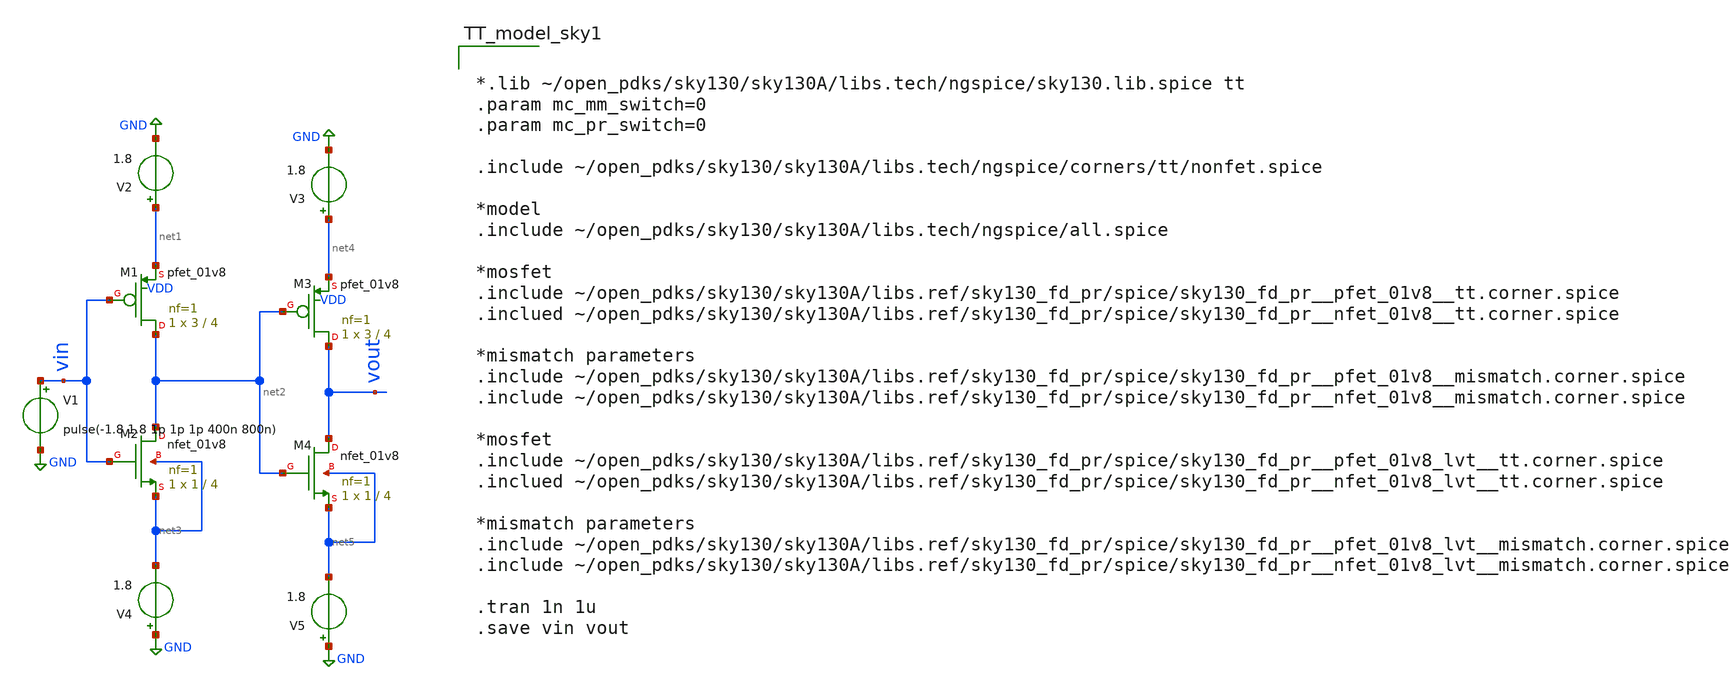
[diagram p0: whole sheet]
** sch_path: buffer.sch
**.subckt buffer
XM1 net2 vin net1 VDD sky130_fd_pr__pfet_01v8 L=4 W=3 nf=1 ad='int((nf+1)/2) * W/nf * 0.29' as='int((nf+2)/2) * W/nf * 0.29'
+ pd='2*int((nf+1)/2) * (W/nf + 0.29)' ps='2*int((nf+2)/2) * (W/nf + 0.29)' nrd='0.29 / W' nrs='0.29 / W'
+ sa=0 sb=0 sd=0 mult=1 m=1
XM2 net2 vin net3 net3 sky130_fd_pr__nfet_01v8 L=4 W=1 nf=1 ad='int((nf+1)/2) * W/nf * 0.29' as='int((nf+2)/2) * W/nf * 0.29'
+ pd='2*int((nf+1)/2) * (W/nf + 0.29)' ps='2*int((nf+2)/2) * (W/nf + 0.29)' nrd='0.29 / W' nrs='0.29 / W'
+ sa=0 sb=0 sd=0 mult=1 m=1
V1 vin GND pulse(-1.8 1.8 1p 1p 1p 400n 800n)
V2 net1 GND 1.8
XM3 vout net2 net4 VDD sky130_fd_pr__pfet_01v8 L=4 W=3 nf=1 ad='int((nf+1)/2) * W/nf * 0.29' as='int((nf+2)/2) * W/nf * 0.29'
+ pd='2*int((nf+1)/2) * (W/nf + 0.29)' ps='2*int((nf+2)/2) * (W/nf + 0.29)' nrd='0.29 / W' nrs='0.29 / W'
+ sa=0 sb=0 sd=0 mult=1 m=1
XM4 vout net2 net5 net5 sky130_fd_pr__nfet_01v8 L=4 W=1 nf=1 ad='int((nf+1)/2) * W/nf * 0.29' as='int((nf+2)/2) * W/nf * 0.29'
+ pd='2*int((nf+1)/2) * (W/nf + 0.29)' ps='2*int((nf+2)/2) * (W/nf + 0.29)' nrd='0.29 / W' nrs='0.29 / W'
+ sa=0 sb=0 sd=0 mult=1 m=1
V3 net4 GND 1.8
V4 GND net3 1.8
V5 GND net5 1.8
**** begin user architecture code

*.lib ~/open_pdks/sky130/sky130A/libs.tech/ngspice/sky130.lib.spice tt
.param mc_mm_switch=0
.param mc_pr_switch=0

.include ~/open_pdks/sky130/sky130A/libs.tech/ngspice/corners/tt/nonfet.spice

*model
.include ~/open_pdks/sky130/sky130A/libs.tech/ngspice/all.spice

*mosfet
.include ~/open_pdks/sky130/sky130A/libs.ref/sky130_fd_pr/spice/sky130_fd_pr__pfet_01v8__tt.corner.spice
.inclued ~/open_pdks/sky130/sky130A/libs.ref/sky130_fd_pr/spice/sky130_fd_pr__nfet_01v8__tt.corner.spice

*mismatch parameters
.include ~/open_pdks/sky130/sky130A/libs.ref/sky130_fd_pr/spice/sky130_fd_pr__pfet_01v8__mismatch.corner.spice
.include ~/open_pdks/sky130/sky130A/libs.ref/sky130_fd_pr/spice/sky130_fd_pr__nfet_01v8__mismatch.corner.spice

*mosfet
.include ~/open_pdks/sky130/sky130A/libs.ref/sky130_fd_pr/spice/sky130_fd_pr__pfet_01v8_lvt__tt.corner.spice
.inclued ~/open_pdks/sky130/sky130A/libs.ref/sky130_fd_pr/spice/sky130_fd_pr__nfet_01v8_lvt__tt.corner.spice

*mismatch parameters
.include ~/open_pdks/sky130/sky130A/libs.ref/sky130_fd_pr/spice/sky130_fd_pr__pfet_01v8_lvt__mismatch.corner.spice
.include ~/open_pdks/sky130/sky130A/libs.ref/sky130_fd_pr/spice/sky130_fd_pr__nfet_01v8_lvt__mismatch.corner.spice

.tran 1n 1u
.save vin vout

**** end user architecture code
**.ends
.GLOBAL GND
.end
